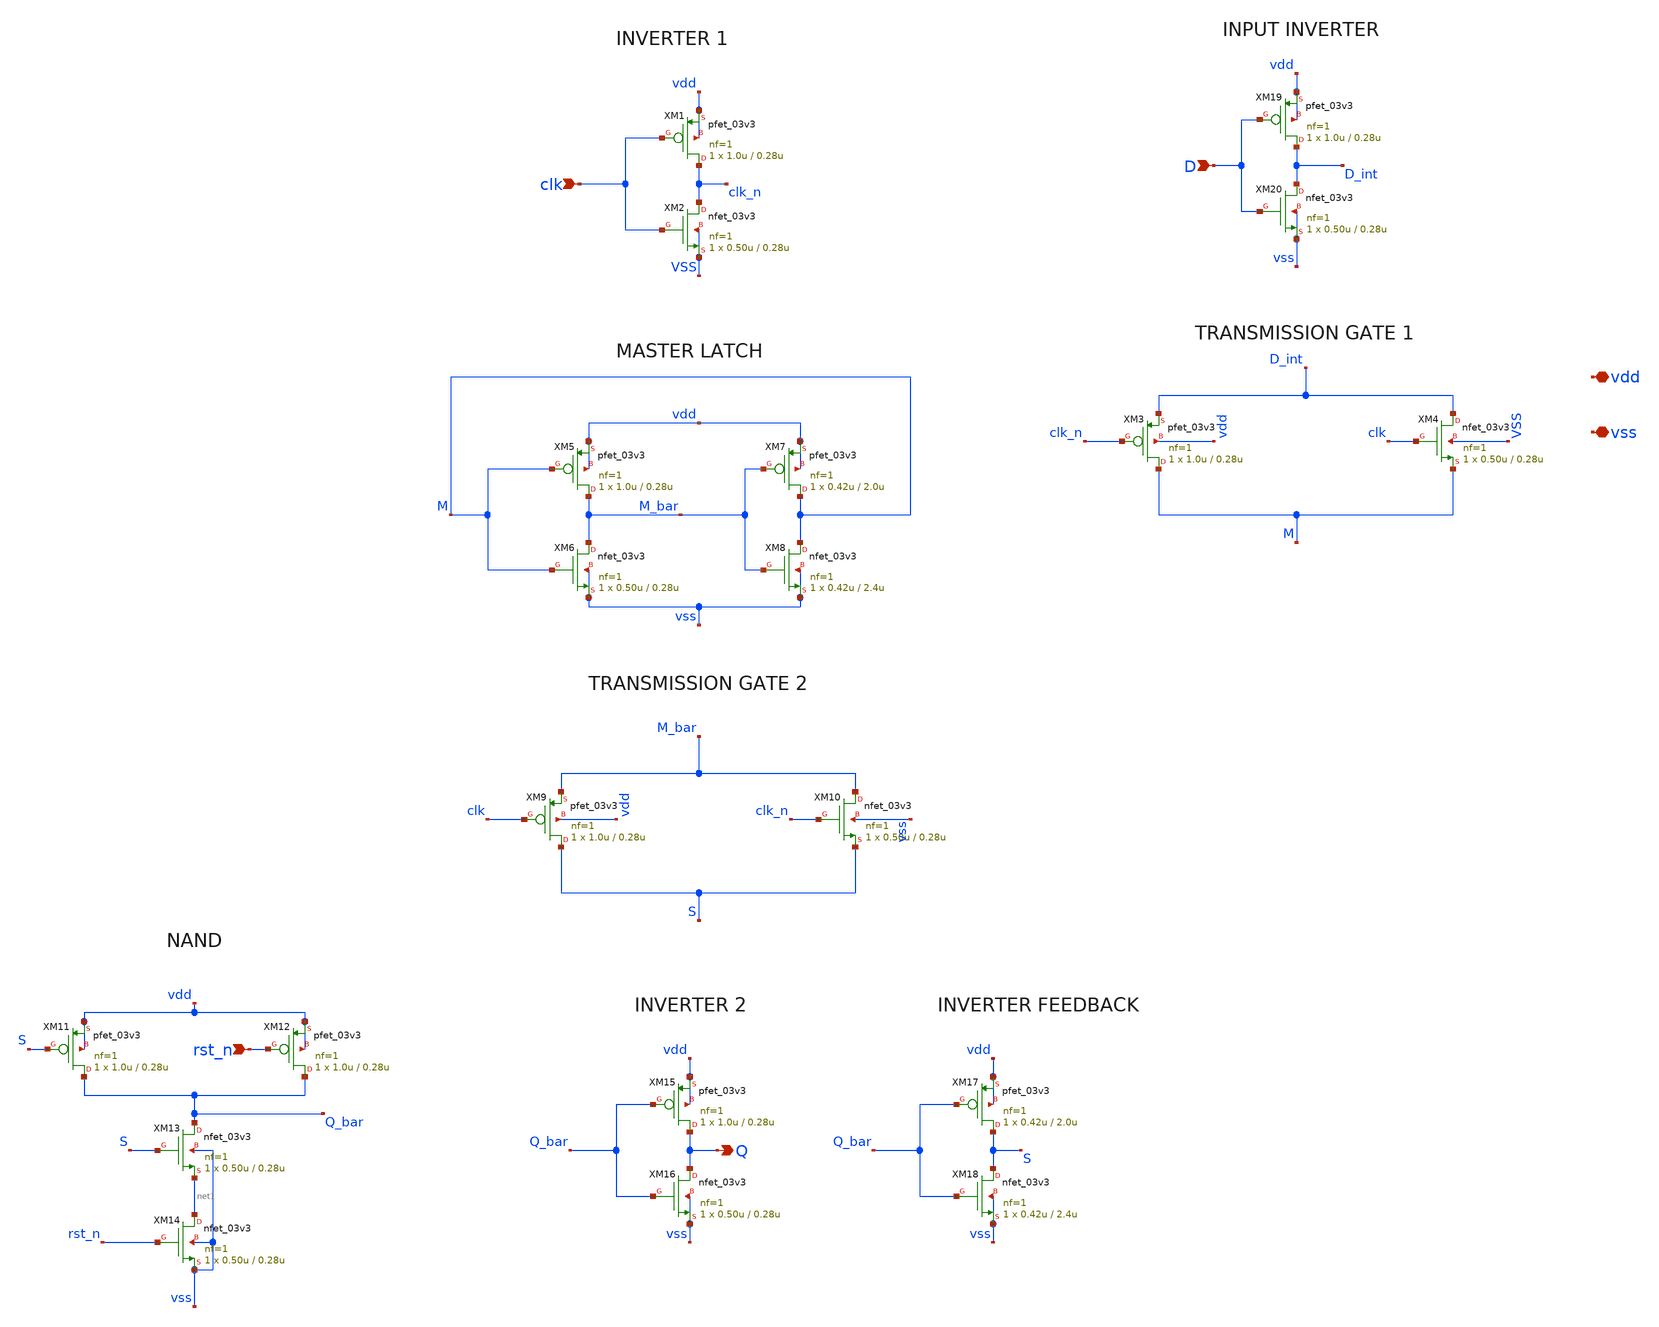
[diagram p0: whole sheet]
** sch_path: xschem/sar_adc/blocks/async_sar/dff_cell.sch
**.subckt dff_cell D clk rst_n Q vdd vss
*.ipin D
*.ipin clk
*.ipin rst_n
*.opin Q
*.iopin vdd
*.iopin vss
XM1 clk_n clk vdd vdd pfet_03v3 L=0.28u W=1.0u nf=1 ad='int((nf+1)/2) * W/nf * 0.18u' as='int((nf+2)/2) * W/nf * 0.18u'
+ pd='2*int((nf+1)/2) * (W/nf + 0.18u)' ps='2*int((nf+2)/2) * (W/nf + 0.18u)' nrd='0.18u / W' nrs='0.18u / W'
+ sa=0 sb=0 sd=0 m=1
XM2 clk_n clk VSS VSS nfet_03v3 L=0.28u W=0.50u nf=1 ad='int((nf+1)/2) * W/nf * 0.18u' as='int((nf+2)/2) * W/nf * 0.18u'
+ pd='2*int((nf+1)/2) * (W/nf + 0.18u)' ps='2*int((nf+2)/2) * (W/nf + 0.18u)' nrd='0.18u / W' nrs='0.18u / W'
+ sa=0 sb=0 sd=0 m=1
XM3 M clk_n D_int vdd pfet_03v3 L=0.28u W=1.0u nf=1 ad='int((nf+1)/2) * W/nf * 0.18u' as='int((nf+2)/2) * W/nf * 0.18u'
+ pd='2*int((nf+1)/2) * (W/nf + 0.18u)' ps='2*int((nf+2)/2) * (W/nf + 0.18u)' nrd='0.18u / W' nrs='0.18u / W'
+ sa=0 sb=0 sd=0 m=1
XM4 D_int clk M VSS nfet_03v3 L=0.28u W=0.50u nf=1 ad='int((nf+1)/2) * W/nf * 0.18u' as='int((nf+2)/2) * W/nf * 0.18u'
+ pd='2*int((nf+1)/2) * (W/nf + 0.18u)' ps='2*int((nf+2)/2) * (W/nf + 0.18u)' nrd='0.18u / W' nrs='0.18u / W'
+ sa=0 sb=0 sd=0 m=1
XM5 M_bar M vdd vdd pfet_03v3 L=0.28u W=1.0u nf=1 ad='int((nf+1)/2) * W/nf * 0.18u' as='int((nf+2)/2) * W/nf * 0.18u'
+ pd='2*int((nf+1)/2) * (W/nf + 0.18u)' ps='2*int((nf+2)/2) * (W/nf + 0.18u)' nrd='0.18u / W' nrs='0.18u / W'
+ sa=0 sb=0 sd=0 m=1
XM6 M_bar M vss vss nfet_03v3 L=0.28u W=0.50u nf=1 ad='int((nf+1)/2) * W/nf * 0.18u' as='int((nf+2)/2) * W/nf * 0.18u'
+ pd='2*int((nf+1)/2) * (W/nf + 0.18u)' ps='2*int((nf+2)/2) * (W/nf + 0.18u)' nrd='0.18u / W' nrs='0.18u / W'
+ sa=0 sb=0 sd=0 m=1
XM7 M M_bar vdd vdd pfet_03v3 L=2.0u W=0.42u nf=1 ad='int((nf+1)/2) * W/nf * 0.18u' as='int((nf+2)/2) * W/nf * 0.18u'
+ pd='2*int((nf+1)/2) * (W/nf + 0.18u)' ps='2*int((nf+2)/2) * (W/nf + 0.18u)' nrd='0.18u / W' nrs='0.18u / W'
+ sa=0 sb=0 sd=0 m=1
XM8 M M_bar vss vss nfet_03v3 L=2.4u W=0.42u nf=1 ad='int((nf+1)/2) * W/nf * 0.18u' as='int((nf+2)/2) * W/nf * 0.18u'
+ pd='2*int((nf+1)/2) * (W/nf + 0.18u)' ps='2*int((nf+2)/2) * (W/nf + 0.18u)' nrd='0.18u / W' nrs='0.18u / W'
+ sa=0 sb=0 sd=0 m=1
XM9 S clk M_bar vdd pfet_03v3 L=0.28u W=1.0u nf=1 ad='int((nf+1)/2) * W/nf * 0.18u' as='int((nf+2)/2) * W/nf * 0.18u'
+ pd='2*int((nf+1)/2) * (W/nf + 0.18u)' ps='2*int((nf+2)/2) * (W/nf + 0.18u)' nrd='0.18u / W' nrs='0.18u / W'
+ sa=0 sb=0 sd=0 m=1
XM10 M_bar clk_n S vss nfet_03v3 L=0.28u W=0.50u nf=1 ad='int((nf+1)/2) * W/nf * 0.18u' as='int((nf+2)/2) * W/nf * 0.18u'
+ pd='2*int((nf+1)/2) * (W/nf + 0.18u)' ps='2*int((nf+2)/2) * (W/nf + 0.18u)' nrd='0.18u / W' nrs='0.18u / W'
+ sa=0 sb=0 sd=0 m=1
XM11 Q_bar S vdd vdd pfet_03v3 L=0.28u W=1.0u nf=1 ad='int((nf+1)/2) * W/nf * 0.18u' as='int((nf+2)/2) * W/nf * 0.18u'
+ pd='2*int((nf+1)/2) * (W/nf + 0.18u)' ps='2*int((nf+2)/2) * (W/nf + 0.18u)' nrd='0.18u / W' nrs='0.18u / W'
+ sa=0 sb=0 sd=0 m=1
XM12 Q_bar rst_n vdd vdd pfet_03v3 L=0.28u W=1.0u nf=1 ad='int((nf+1)/2) * W/nf * 0.18u' as='int((nf+2)/2) * W/nf * 0.18u'
+ pd='2*int((nf+1)/2) * (W/nf + 0.18u)' ps='2*int((nf+2)/2) * (W/nf + 0.18u)' nrd='0.18u / W' nrs='0.18u / W'
+ sa=0 sb=0 sd=0 m=1
XM13 Q_bar S net1 vss nfet_03v3 L=0.28u W=0.50u nf=1 ad='int((nf+1)/2) * W/nf * 0.18u' as='int((nf+2)/2) * W/nf * 0.18u'
+ pd='2*int((nf+1)/2) * (W/nf + 0.18u)' ps='2*int((nf+2)/2) * (W/nf + 0.18u)' nrd='0.18u / W' nrs='0.18u / W'
+ sa=0 sb=0 sd=0 m=1
XM14 net1 rst_n vss vss nfet_03v3 L=0.28u W=0.50u nf=1 ad='int((nf+1)/2) * W/nf * 0.18u' as='int((nf+2)/2) * W/nf * 0.18u'
+ pd='2*int((nf+1)/2) * (W/nf + 0.18u)' ps='2*int((nf+2)/2) * (W/nf + 0.18u)' nrd='0.18u / W' nrs='0.18u / W'
+ sa=0 sb=0 sd=0 m=1
XM15 Q Q_bar vdd vdd pfet_03v3 L=0.28u W=1.0u nf=1 ad='int((nf+1)/2) * W/nf * 0.18u' as='int((nf+2)/2) * W/nf * 0.18u'
+ pd='2*int((nf+1)/2) * (W/nf + 0.18u)' ps='2*int((nf+2)/2) * (W/nf + 0.18u)' nrd='0.18u / W' nrs='0.18u / W'
+ sa=0 sb=0 sd=0 m=1
XM16 Q Q_bar vss vss nfet_03v3 L=0.28u W=0.50u nf=1 ad='int((nf+1)/2) * W/nf * 0.18u' as='int((nf+2)/2) * W/nf * 0.18u'
+ pd='2*int((nf+1)/2) * (W/nf + 0.18u)' ps='2*int((nf+2)/2) * (W/nf + 0.18u)' nrd='0.18u / W' nrs='0.18u / W'
+ sa=0 sb=0 sd=0 m=1
XM17 S Q_bar vdd vdd pfet_03v3 L=2.0u W=0.42u nf=1 ad='int((nf+1)/2) * W/nf * 0.18u' as='int((nf+2)/2) * W/nf * 0.18u'
+ pd='2*int((nf+1)/2) * (W/nf + 0.18u)' ps='2*int((nf+2)/2) * (W/nf + 0.18u)' nrd='0.18u / W' nrs='0.18u / W'
+ sa=0 sb=0 sd=0 m=1
XM18 S Q_bar vss vss nfet_03v3 L=2.4u W=0.42u nf=1 ad='int((nf+1)/2) * W/nf * 0.18u' as='int((nf+2)/2) * W/nf * 0.18u'
+ pd='2*int((nf+1)/2) * (W/nf + 0.18u)' ps='2*int((nf+2)/2) * (W/nf + 0.18u)' nrd='0.18u / W' nrs='0.18u / W'
+ sa=0 sb=0 sd=0 m=1
XM19 D_int D vdd vdd pfet_03v3 L=0.28u W=1.0u nf=1 ad='int((nf+1)/2) * W/nf * 0.18u' as='int((nf+2)/2) * W/nf * 0.18u'
+ pd='2*int((nf+1)/2) * (W/nf + 0.18u)' ps='2*int((nf+2)/2) * (W/nf + 0.18u)' nrd='0.18u / W' nrs='0.18u / W'
+ sa=0 sb=0 sd=0 m=1
XM20 D_int D vss vss nfet_03v3 L=0.28u W=0.50u nf=1 ad='int((nf+1)/2) * W/nf * 0.18u' as='int((nf+2)/2) * W/nf * 0.18u'
+ pd='2*int((nf+1)/2) * (W/nf + 0.18u)' ps='2*int((nf+2)/2) * (W/nf + 0.18u)' nrd='0.18u / W' nrs='0.18u / W'
+ sa=0 sb=0 sd=0 m=1
**.ends
.end
